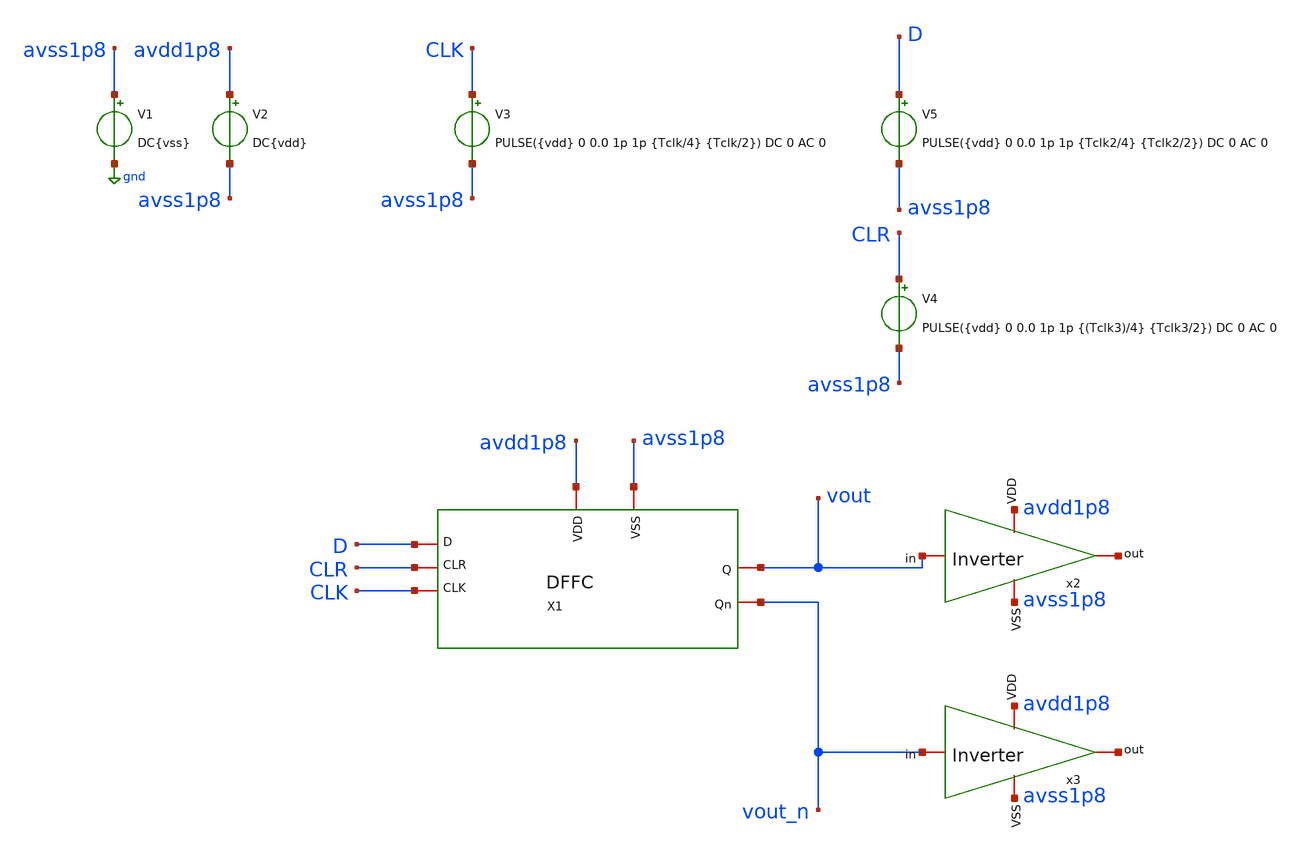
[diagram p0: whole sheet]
** sch_path: verification/testbenches/tb_dffc.sch
**.subckt tb_dffc
V1 avss1p8 gnd DC{vss}
V2 avdd1p8 avss1p8 DC{vdd}
V3 CLK avss1p8 PULSE({vdd} 0 0.0 1p 1p {Tclk/4} {Tclk/2}) DC 0 AC 0
V4 CLR avss1p8 PULSE({vdd} 0 0.0 1p 1p {(Tclk3)/4} {Tclk3/2}) DC 0 AC 0
x2 avdd1p8 net1 vout avss1p8 inverter
x1 D avdd1p8 avss1p8 vout CLK CLR vout_n dffc
V5 D avss1p8 PULSE({vdd} 0 0.0 1p 1p {Tclk2/4} {Tclk2/2}) DC 0 AC 0
x3 avdd1p8 net2 vout_n avss1p8 inverter
**** begin user architecture code


* Circuit Parameters
.param vdd = 1.2
.param vss = 0.0
.param Tclk = 10n
.param Tclk2 = 3n
.param Tclk3 = 100n
.options TEMP = 27.0
* Include Models - IHP SG13G2
.lib cornerMOSlv.lib mos_tt
* OP Parameters & Singals to save
.save all
*Simulations
.control
tran 0.01u 40n
setplot tran1
plot v(CLK) v(CLR)+1.2 v(D)+2.4 v(vout)+3.6 v(vout_n)+4.8
reset
set filetype = ascii
write dcsweep.raw
.endc
.end


**** end user architecture code
**.ends
.GLOBAL gnd
.end
